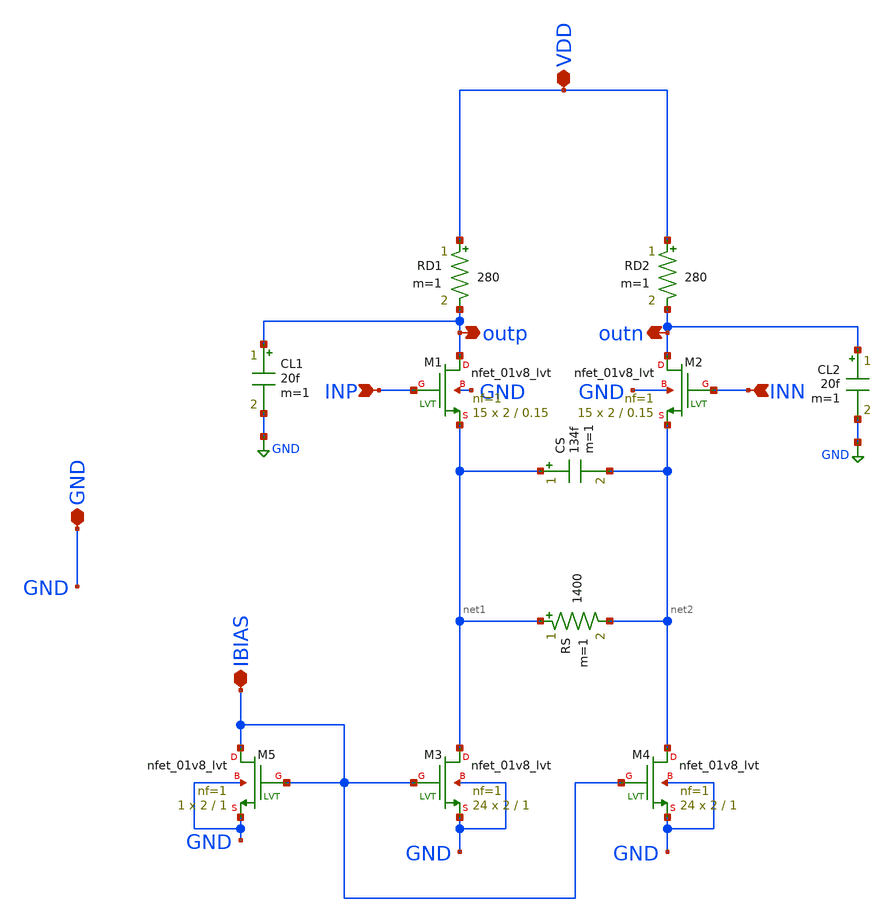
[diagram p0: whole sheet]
** sch_path: CTLE/ctle_sym.sch
**.subckt ctle_sym outp outn INN VDD GND IBIAS INP
*.opin outp
*.opin outn
*.ipin INN
*.iopin VDD
*.iopin GND
*.iopin IBIAS
*.ipin INP
XM1 outp INP net1 GND sky130_fd_pr__nfet_01v8_lvt L=0.15 W=2 nf=1 ad='int((nf+1)/2) * W/nf * 0.29' as='int((nf+2)/2) * W/nf * 0.29'
+ pd='2*int((nf+1)/2) * (W/nf + 0.29)' ps='2*int((nf+2)/2) * (W/nf + 0.29)' nrd='0.29 / W' nrs='0.29 / W'
+ sa=0 sb=0 sd=0 mult=15 m=15
XM2 outn INN net2 GND sky130_fd_pr__nfet_01v8_lvt L=0.15 W=2 nf=1 ad='int((nf+1)/2) * W/nf * 0.29' as='int((nf+2)/2) * W/nf * 0.29'
+ pd='2*int((nf+1)/2) * (W/nf + 0.29)' ps='2*int((nf+2)/2) * (W/nf + 0.29)' nrd='0.29 / W' nrs='0.29 / W'
+ sa=0 sb=0 sd=0 mult=15 m=15
XM3 net1 IBIAS GND GND sky130_fd_pr__nfet_01v8_lvt L=1 W=2 nf=1 ad='int((nf+1)/2) * W/nf * 0.29' as='int((nf+2)/2) * W/nf * 0.29'
+ pd='2*int((nf+1)/2) * (W/nf + 0.29)' ps='2*int((nf+2)/2) * (W/nf + 0.29)' nrd='0.29 / W' nrs='0.29 / W'
+ sa=0 sb=0 sd=0 mult=24 m=24
XM4 net2 IBIAS GND GND sky130_fd_pr__nfet_01v8_lvt L=1 W=2 nf=1 ad='int((nf+1)/2) * W/nf * 0.29' as='int((nf+2)/2) * W/nf * 0.29'
+ pd='2*int((nf+1)/2) * (W/nf + 0.29)' ps='2*int((nf+2)/2) * (W/nf + 0.29)' nrd='0.29 / W' nrs='0.29 / W'
+ sa=0 sb=0 sd=0 mult=24 m=24
XM5 IBIAS IBIAS GND GND sky130_fd_pr__nfet_01v8_lvt L=1 W=2 nf=1 ad='int((nf+1)/2) * W/nf * 0.29' as='int((nf+2)/2) * W/nf * 0.29'
+ pd='2*int((nf+1)/2) * (W/nf + 0.29)' ps='2*int((nf+2)/2) * (W/nf + 0.29)' nrd='0.29 / W' nrs='0.29 / W'
+ sa=0 sb=0 sd=0 mult=1 m=1
RD1 VDD outp 280 m=1
RD2 VDD outn 280 m=1
CS net1 net2 134f m=1
RS net1 net2 1400 m=1
CL1 outp GND 20f m=1
CL2 outn GND 20f m=1
**.ends
.GLOBAL GND
.end
